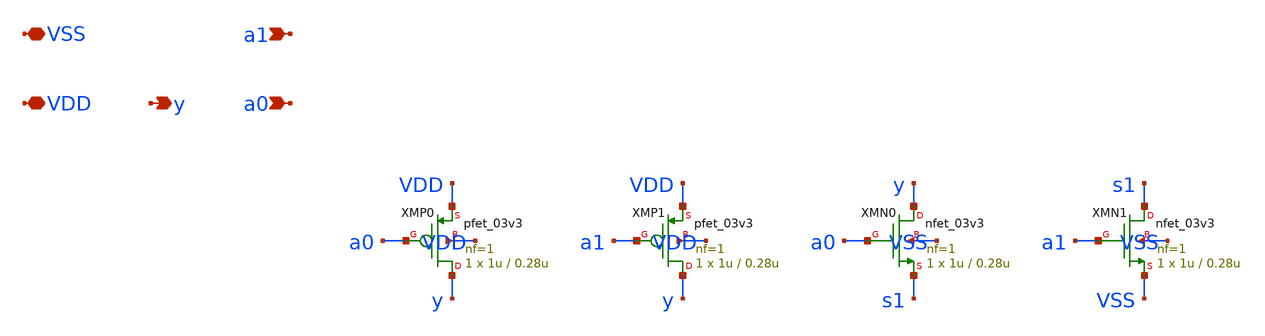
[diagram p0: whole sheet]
** sch_path: design/nand2.sch
**.subckt nand2 a0 a1 y VDD VSS
*.ipin a0
*.ipin a1
*.opin y
*.iopin VDD
*.iopin VSS
XMP0 y a0 VDD VDD pfet_03v3 L=0.28u W=1u nf=1 ad='int((nf+1)/2) * W/nf * 0.18u' as='int((nf+2)/2) * W/nf * 0.18u'
+ pd='2*int((nf+1)/2) * (W/nf + 0.18u)' ps='2*int((nf+2)/2) * (W/nf + 0.18u)' nrd='0.18u / W' nrs='0.18u / W'
+ sa=0 sb=0 sd=0 m=1
XMP1 y a1 VDD VDD pfet_03v3 L=0.28u W=1u nf=1 ad='int((nf+1)/2) * W/nf * 0.18u' as='int((nf+2)/2) * W/nf * 0.18u'
+ pd='2*int((nf+1)/2) * (W/nf + 0.18u)' ps='2*int((nf+2)/2) * (W/nf + 0.18u)' nrd='0.18u / W' nrs='0.18u / W'
+ sa=0 sb=0 sd=0 m=1
XMN0 y a0 s1 VSS nfet_03v3 L=0.28u W=1u nf=1 ad='int((nf+1)/2) * W/nf * 0.18u' as='int((nf+2)/2) * W/nf * 0.18u'
+ pd='2*int((nf+1)/2) * (W/nf + 0.18u)' ps='2*int((nf+2)/2) * (W/nf + 0.18u)' nrd='0.18u / W' nrs='0.18u / W'
+ sa=0 sb=0 sd=0 m=1
XMN1 s1 a1 VSS VSS nfet_03v3 L=0.28u W=1u nf=1 ad='int((nf+1)/2) * W/nf * 0.18u' as='int((nf+2)/2) * W/nf * 0.18u'
+ pd='2*int((nf+1)/2) * (W/nf + 0.18u)' ps='2*int((nf+2)/2) * (W/nf + 0.18u)' nrd='0.18u / W' nrs='0.18u / W'
+ sa=0 sb=0 sd=0 m=1
**.ends
.end
